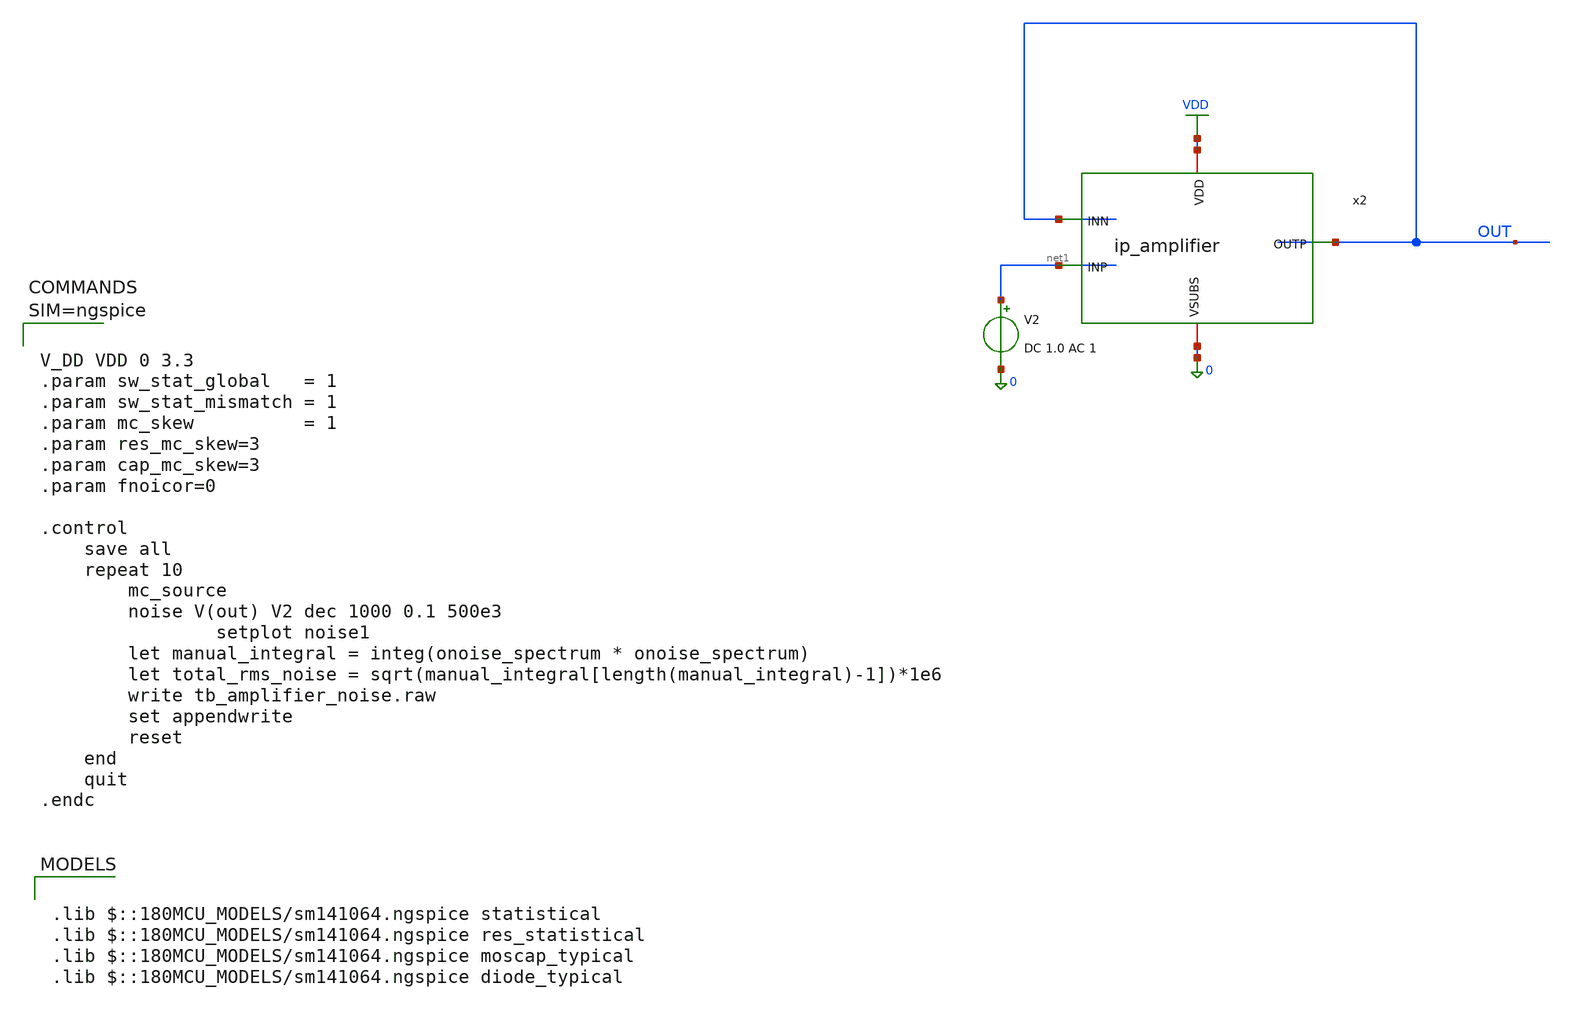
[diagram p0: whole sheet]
** sch_path: xschem/tb_amplifier_noise.sch
**.subckt tb_amplifier_noise
V2 net1 0 DC 1.0 AC 1
x2 VDD OUT net1 OUT 0 ip_amplifier
**** begin user architecture code

.lib $::180MCU_MODELS/sm141064.ngspice statistical
.lib $::180MCU_MODELS/sm141064.ngspice res_statistical
.lib $::180MCU_MODELS/sm141064.ngspice moscap_typical
.lib $::180MCU_MODELS/sm141064.ngspice diode_typical




V_DD VDD 0 3.3
.param sw_stat_global   = 1
.param sw_stat_mismatch = 1
.param mc_skew          = 1
.param res_mc_skew=3
.param cap_mc_skew=3
.param fnoicor=0

.control
	save all
	repeat 10
		mc_source
		noise V(out) V2 dec 1000 0.1 500e3
                setplot noise1
		let manual_integral = integ(onoise_spectrum * onoise_spectrum)
		let total_rms_noise = sqrt(manual_integral[length(manual_integral)-1])*1e6
		write tb_amplifier_noise.raw
		set appendwrite
		reset
	end
	quit
.endc



**** end user architecture code
**.ends

* expanding   symbol:  ip_amplifier.sym # of pins=5
** sym_path: xschem/ip_amplifier.sym
** sch_path: xschem/ip_amplifier.sch
.subckt ip_amplifier VDD OUTP INP INN VSUBS
*.iopin VDD
*.iopin VSUBS
*.ipin INP
*.ipin INN
*.opin OUTP
XM1 COMP INP COMMON_ VDD pfet_03v3 L=5u W=18.0u nf=1 ad='int((nf+1)/2) * W/nf * 0.18u' as='int((nf+2)/2) * W/nf * 0.18u'
+ pd='2*int((nf+1)/2) * (W/nf + 0.18u)' ps='2*int((nf+2)/2) * (W/nf + 0.18u)' nrd='0.18u / W' nrs='0.18u / W'
+ sa=0 sb=0 sd=0 m=1 par=1
XM2 net6 INN COMMON_ VDD pfet_03v3 L=5u W=18.0u nf=1 ad='int((nf+1)/2) * W/nf * 0.18u' as='int((nf+2)/2) * W/nf * 0.18u'
+ pd='2*int((nf+1)/2) * (W/nf + 0.18u)' ps='2*int((nf+2)/2) * (W/nf + 0.18u)' nrd='0.18u / W' nrs='0.18u / W'
+ sa=0 sb=0 sd=0 m=1 par=1
XM3 net2 NBIAS VSUBS vsubs nfet_03v3 L=2u W=6u nf=1 ad='int((nf+1)/2) * W/nf * 0.18u' as='int((nf+2)/2) * W/nf * 0.18u'
+ pd='2*int((nf+1)/2) * (W/nf + 0.18u)' ps='2*int((nf+2)/2) * (W/nf + 0.18u)' nrd='0.18u / W' nrs='0.18u / W'
+ sa=0 sb=0 sd=0 m=2 par=2
XM4 net1 NBIAS VSUBS vsubs nfet_03v3 L=2u W=6u nf=1 ad='int((nf+1)/2) * W/nf * 0.18u' as='int((nf+2)/2) * W/nf * 0.18u'
+ pd='2*int((nf+1)/2) * (W/nf + 0.18u)' ps='2*int((nf+2)/2) * (W/nf + 0.18u)' nrd='0.18u / W' nrs='0.18u / W'
+ sa=0 sb=0 sd=0 m=1 par=1
XM7 NBIAS NBIAS net2 vsubs nfet_03v3 L=0.5u W=6u nf=1 ad='int((nf+1)/2) * W/nf * 0.18u' as='int((nf+2)/2) * W/nf * 0.18u'
+ pd='2*int((nf+1)/2) * (W/nf + 0.18u)' ps='2*int((nf+2)/2) * (W/nf + 0.18u)' nrd='0.18u / W' nrs='0.18u / W'
+ sa=0 sb=0 sd=0 m=4 par=4
XM8 net3 NBIAS net1 vsubs nfet_03v3 L=0.5u W=6u nf=1 ad='int((nf+1)/2) * W/nf * 0.18u' as='int((nf+2)/2) * W/nf * 0.18u'
+ pd='2*int((nf+1)/2) * (W/nf + 0.18u)' ps='2*int((nf+2)/2) * (W/nf + 0.18u)' nrd='0.18u / W' nrs='0.18u / W'
+ sa=0 sb=0 sd=0 m=4 par=4
XM9 net4 PBIAS VDD VDD pfet_03v3 L=2u W=6u nf=1 ad='int((nf+1)/2) * W/nf * 0.18u' as='int((nf+2)/2) * W/nf * 0.18u'
+ pd='2*int((nf+1)/2) * (W/nf + 0.18u)' ps='2*int((nf+2)/2) * (W/nf + 0.18u)' nrd='0.18u / W' nrs='0.18u / W'
+ sa=0 sb=0 sd=0 m=1 par=1
XM10 net5 PBIAS VDD VDD pfet_03v3 L=2u W=6u nf=1 ad='int((nf+1)/2) * W/nf * 0.18u' as='int((nf+2)/2) * W/nf * 0.18u'
+ pd='2*int((nf+1)/2) * (W/nf + 0.18u)' ps='2*int((nf+2)/2) * (W/nf + 0.18u)' nrd='0.18u / W' nrs='0.18u / W'
+ sa=0 sb=0 sd=0 m=1 par=1
XM11 PBIAS PBIAS net4 VDD pfet_03v3 L=0.5u W=6u nf=1 ad='int((nf+1)/2) * W/nf * 0.18u' as='int((nf+2)/2) * W/nf * 0.18u'
+ pd='2*int((nf+1)/2) * (W/nf + 0.18u)' ps='2*int((nf+2)/2) * (W/nf + 0.18u)' nrd='0.18u / W' nrs='0.18u / W'
+ sa=0 sb=0 sd=0 m=4 par=4
XM12 COMMON PBIAS net5 VDD pfet_03v3 L=0.5u W=6u nf=1 ad='int((nf+1)/2) * W/nf * 0.18u' as='int((nf+2)/2) * W/nf * 0.18u'
+ pd='2*int((nf+1)/2) * (W/nf + 0.18u)' ps='2*int((nf+2)/2) * (W/nf + 0.18u)' nrd='0.18u / W' nrs='0.18u / W'
+ sa=0 sb=0 sd=0 m=4 par=4
XM13 COMP net6 VSUBS vsubs nfet_03v3 L=5u W=6u nf=1 ad='int((nf+1)/2) * W/nf * 0.18u' as='int((nf+2)/2) * W/nf * 0.18u'
+ pd='2*int((nf+1)/2) * (W/nf + 0.18u)' ps='2*int((nf+2)/2) * (W/nf + 0.18u)' nrd='0.18u / W' nrs='0.18u / W'
+ sa=0 sb=0 sd=0 m=1 par=1
XM14 net6 net6 VSUBS vsubs nfet_03v3 L=5u W=6u nf=1 ad='int((nf+1)/2) * W/nf * 0.18u' as='int((nf+2)/2) * W/nf * 0.18u'
+ pd='2*int((nf+1)/2) * (W/nf + 0.18u)' ps='2*int((nf+2)/2) * (W/nf + 0.18u)' nrd='0.18u / W' nrs='0.18u / W'
+ sa=0 sb=0 sd=0 m=1 par=1
XM17 net8 PBIAS VDD VDD pfet_03v3 L=0.5u W=12u nf=1 ad='int((nf+1)/2) * W/nf * 0.18u' as='int((nf+2)/2) * W/nf * 0.18u'
+ pd='2*int((nf+1)/2) * (W/nf + 0.18u)' ps='2*int((nf+2)/2) * (W/nf + 0.18u)' nrd='0.18u / W' nrs='0.18u / W'
+ sa=0 sb=0 sd=0 m=2 par=2
XM18 OUTP COMP VSUBS vsubs nfet_03v3 L=0.5u W=12u nf=1 ad='int((nf+1)/2) * W/nf * 0.18u' as='int((nf+2)/2) * W/nf * 0.18u'
+ pd='2*int((nf+1)/2) * (W/nf + 0.18u)' ps='2*int((nf+2)/2) * (W/nf + 0.18u)' nrd='0.18u / W' nrs='0.18u / W'
+ sa=0 sb=0 sd=0 m=4 par=4
XR3 NBIAS net7 vsubs ppolyf_u_1k r_width=1e-6 r_length=48e-6 m=1
Vmeas VDD net7 0
Vmeas1 PBIAS net3 0
XC1 OUTP net9 cap_pmos_03v3 c_width=13.5e-6 c_length=18e-6 m=1
XC2 COMP net9 cap_pmos_03v3 c_width=13.5e-6 c_length=18e-6 m=1
Vmeas2 COMMON COMMON_ 0
Vmeas3 net8 OUTP 0
XR2 VDD net9 vsubs ppolyf_u_1k r_width=1e-6 r_length=96e-6 m=1
.ends

.GLOBAL VDD
.end
